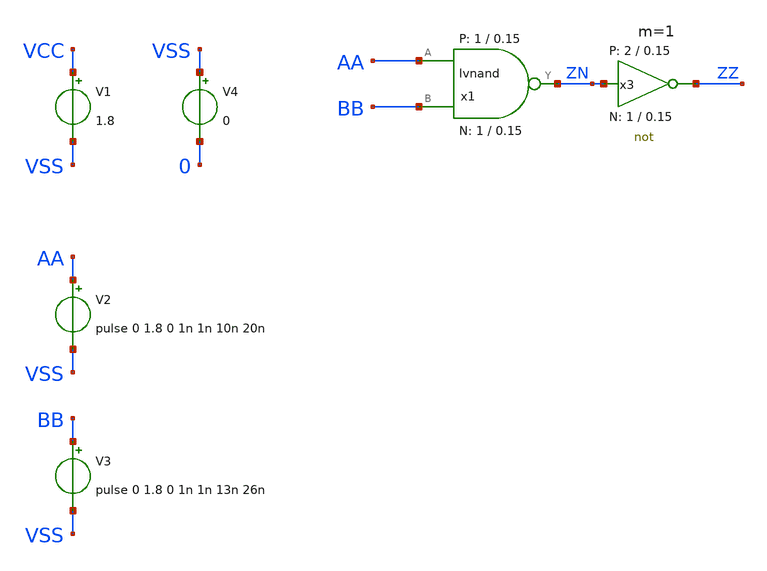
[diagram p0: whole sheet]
** sch_path: sky130A/xschem_libs/sky130_tests_ase/logic_ngspice/schematic/logic_ngspice.sch
* Copyright 2021 Stefan Frederik Schippers
* Licensed under the Apache License, Version 2.0 (the "License");
* you may not use this file except in compliance with the License.
* You may obtain a copy of the License at
* https://www.apache.org/licenses/LICENSE-2.0
* Unless required by applicable law or agreed to in writing, software
* distributed under the License is distributed on an "AS IS" BASIS,
* WITHOUT WARRANTIES OR CONDITIONS OF ANY KIND, either express or implied.
* See the License for the specific language governing permissions and
* limitations under the License.
**.subckt logic_ngspice
x1 AA BB ZN VCC VSS lvnand WidthN=1 LenN=0.15 WidthP=1 LenP=0.15 m=1
V1 VCC VSS 1.8
V2 AA VSS pulse 0 1.8 0 1n 1n 10n 20n
V3 BB VSS pulse 0 1.8 0 1n 1n 13n 26n
x3 ZZ ZN VCC VSS not W_N=1 L_N=0.15 W_P=2 L_P=0.15 m=1
V4 VSS 0 0
**.ends
.end
